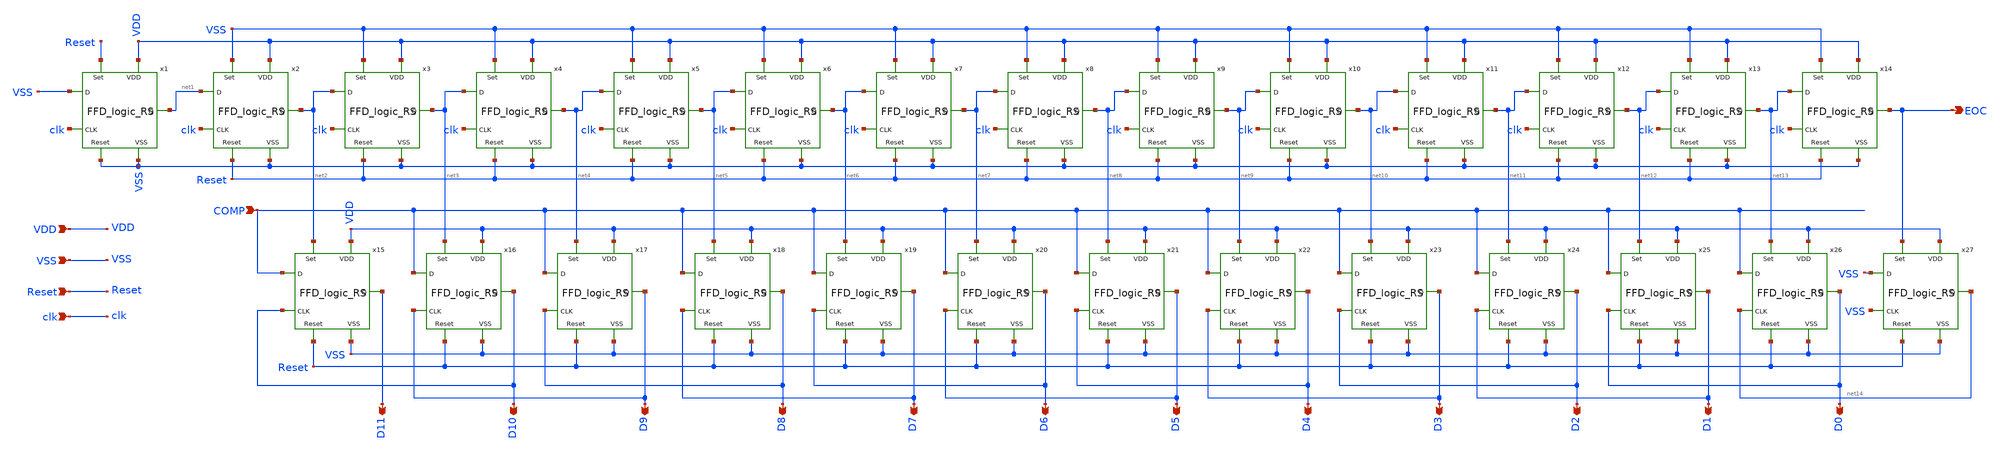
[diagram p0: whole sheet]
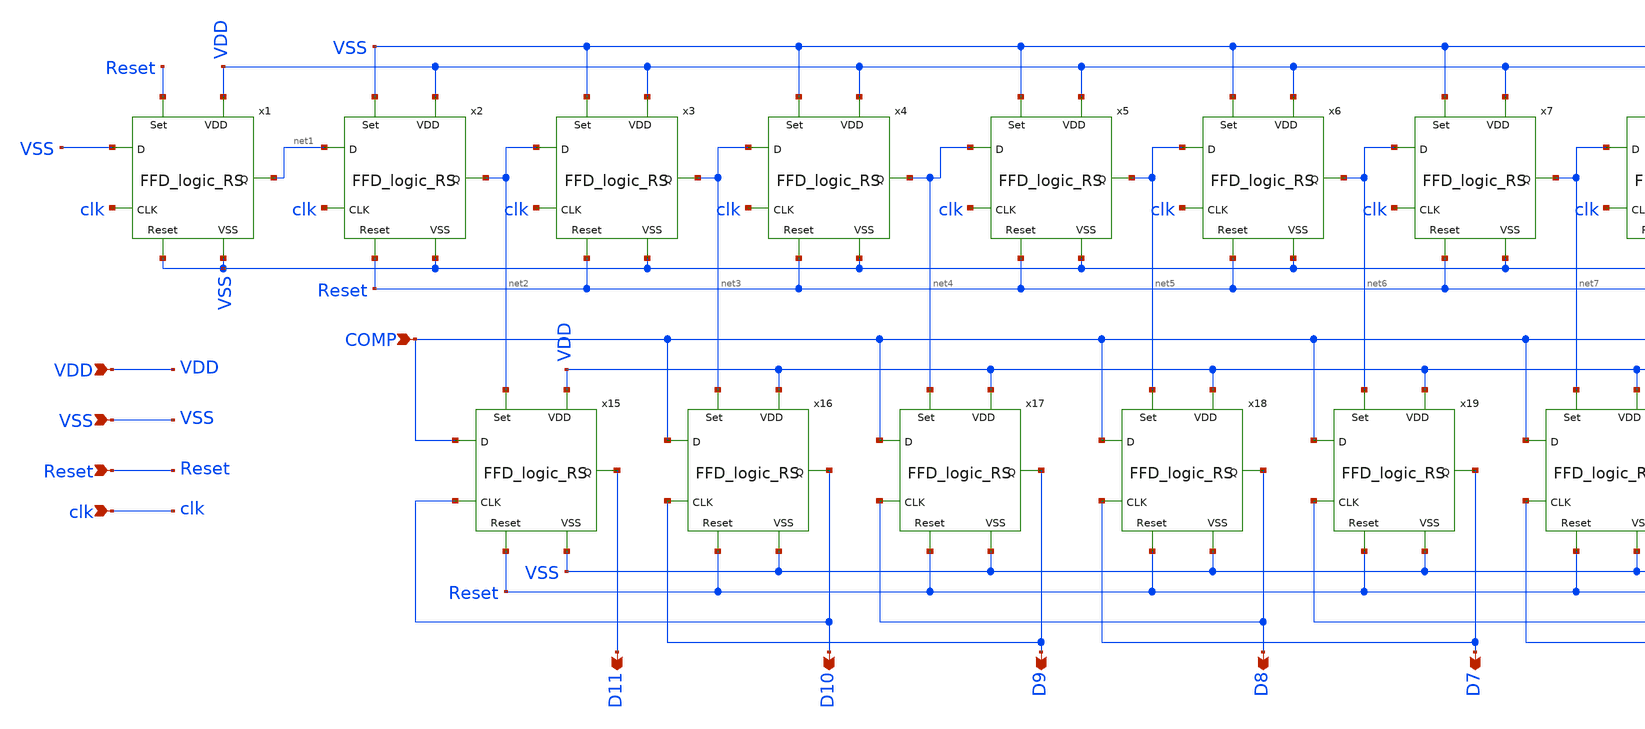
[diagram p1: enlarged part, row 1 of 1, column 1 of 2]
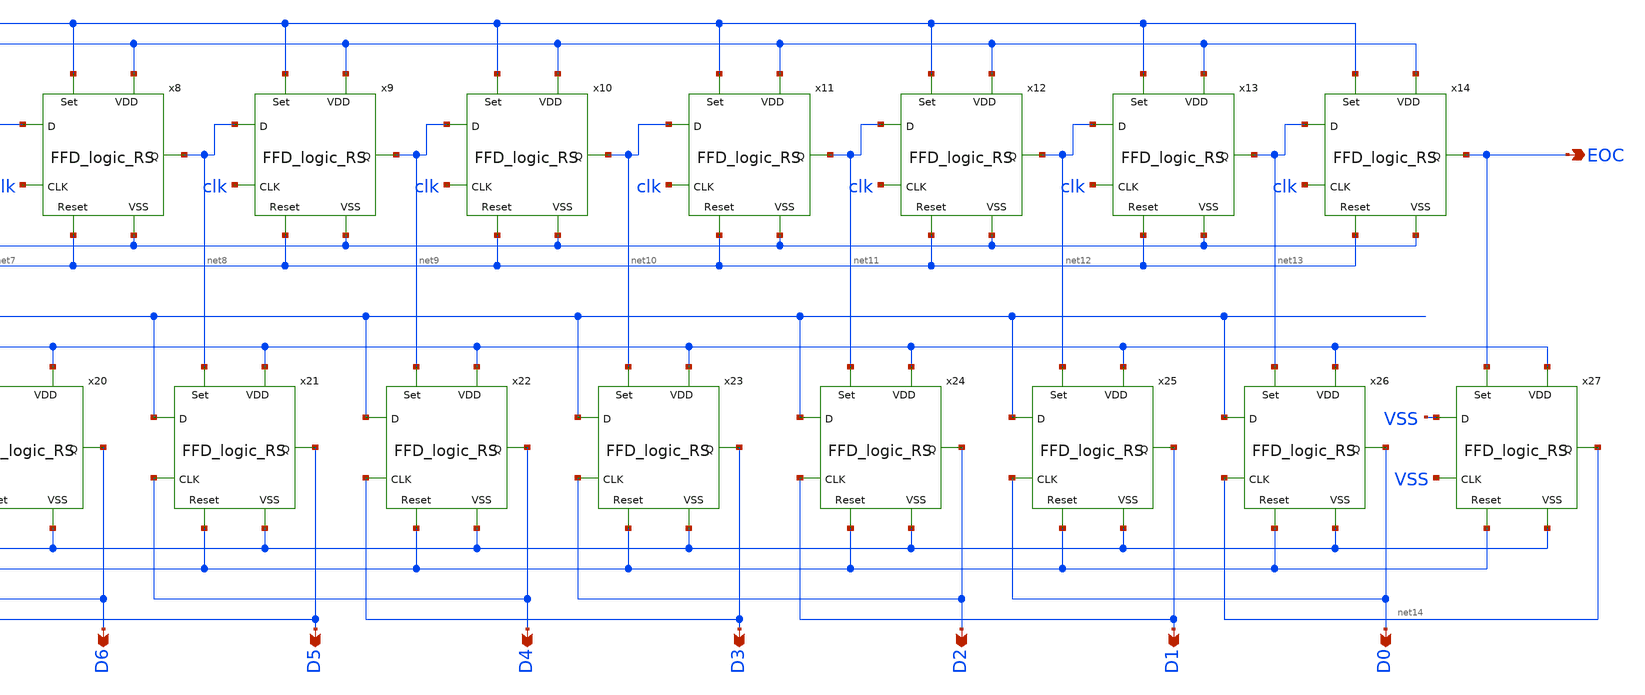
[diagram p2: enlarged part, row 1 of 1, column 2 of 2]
** sch_path: SAR_Logic_new.sch
**.subckt SAR_Logic_new VDD VSS COMP Reset clk D11 D10 D9 D8 D7 D6 D5 D4 D3 D2 D1 D0 EOC
*.ipin VDD
*.ipin VSS
*.ipin COMP
*.ipin Reset
*.ipin clk
*.opin D11
*.opin D10
*.opin D9
*.opin D8
*.opin D7
*.opin D6
*.opin D5
*.opin D4
*.opin D3
*.opin D2
*.opin D1
*.opin D0
*.opin EOC
x1 Reset VDD net1 clk VSS VSS VSS FFD_logic_RS
x2 VSS VDD net2 clk net1 VSS Reset FFD_logic_RS
x3 VSS VDD net3 clk net2 VSS Reset FFD_logic_RS
x4 VSS VDD net4 clk net3 VSS Reset FFD_logic_RS
x5 VSS VDD net5 clk net4 VSS Reset FFD_logic_RS
x6 VSS VDD net6 clk net5 VSS Reset FFD_logic_RS
x7 VSS VDD net7 clk net6 VSS Reset FFD_logic_RS
x8 VSS VDD net8 clk net7 VSS Reset FFD_logic_RS
x9 VSS VDD net9 clk net8 VSS Reset FFD_logic_RS
x10 VSS VDD net10 clk net9 VSS Reset FFD_logic_RS
x11 VSS VDD net11 clk net10 VSS Reset FFD_logic_RS
x12 VSS VDD net12 clk net11 VSS Reset FFD_logic_RS
x13 VSS VDD net13 clk net12 VSS Reset FFD_logic_RS
x14 VSS VDD EOC clk net13 VSS Reset FFD_logic_RS
x15 net2 VDD D11 D10 COMP VSS Reset FFD_logic_RS
x16 net3 VDD D10 D9 COMP VSS Reset FFD_logic_RS
x17 net4 VDD D9 D8 COMP VSS Reset FFD_logic_RS
x18 net5 VDD D8 D7 COMP VSS Reset FFD_logic_RS
x19 net6 VDD D7 D6 COMP VSS Reset FFD_logic_RS
x20 net7 VDD D6 D5 COMP VSS Reset FFD_logic_RS
x21 net8 VDD D5 D4 COMP VSS Reset FFD_logic_RS
x22 net9 VDD D4 D3 COMP VSS Reset FFD_logic_RS
x23 net10 VDD D3 D2 COMP VSS Reset FFD_logic_RS
x24 net11 VDD D2 D1 COMP VSS Reset FFD_logic_RS
x25 net12 VDD D1 D0 COMP VSS Reset FFD_logic_RS
x26 net13 VDD D0 net14 COMP VSS Reset FFD_logic_RS
x27 EOC VDD net14 VSS VSS VSS Reset FFD_logic_RS
**.ends

* expanding   symbol:  Thesis/FFD_logic_RS.sym # of pins=7
** sym_path: FFD_logic_RS.sym
** sch_path: FFD_logic_RS.sch
.subckt FFD_logic_RS Set VDD Q CLK D VSS Reset
*.ipin D
*.ipin CLK
*.ipin VDD
*.ipin VSS
*.opin Q
*.ipin Set
*.ipin Reset
x1 VDD net3 D net2 VSS nand_FFD
x2 VDD net4 net2 net1 VSS nand_FFD
x5 VDD net8 net5 CLK VSS nand_FFD
x6 VDD net7 CLK net6 VSS nand_FFD
x9 VDD D net1 VSS Inverter
x10 VDD CLK net2 VSS Inverter
x3 net6 VDD net5 net10 net3 VSS nand_FFD_3pin
x4 net11 VDD net6 net5 net4 VSS nand_FFD_3pin
x7 net9 VDD Q net10 net8 VSS nand_FFD_3pin
x8 net11 VDD net9 Q net7 VSS nand_FFD_3pin
x11 VDD Set net10 VSS Inverter
x12 VDD Reset net11 VSS Inverter
.ends


* expanding   symbol:  nand_FFD.sym # of pins=5
** sym_path: nand_FFD.sym
** sch_path: nand_FFD.sch
.subckt nand_FFD VDD Y A B VSS
*.ipin VDD
*.ipin A
*.ipin B
*.ipin VSS
*.opin Y
XM1 Y A net1 VSS sky130_fd_pr__nfet_01v8 L=0.15 W=1 nf=1 ad='int((nf+1)/2) * W/nf * 0.29' as='int((nf+2)/2) * W/nf * 0.29'
+ pd='2*int((nf+1)/2) * (W/nf + 0.29)' ps='2*int((nf+2)/2) * (W/nf + 0.29)' nrd='0.29 / W' nrs='0.29 / W'
+ sa=0 sb=0 sd=0 mult=1 m=1
XM2 net1 B VSS VSS sky130_fd_pr__nfet_01v8 L=0.15 W=1 nf=1 ad='int((nf+1)/2) * W/nf * 0.29' as='int((nf+2)/2) * W/nf * 0.29'
+ pd='2*int((nf+1)/2) * (W/nf + 0.29)' ps='2*int((nf+2)/2) * (W/nf + 0.29)' nrd='0.29 / W' nrs='0.29 / W'
+ sa=0 sb=0 sd=0 mult=1 m=1
XM3 Y A VDD VDD sky130_fd_pr__pfet_01v8 L=0.15 W=2 nf=1 ad='int((nf+1)/2) * W/nf * 0.29' as='int((nf+2)/2) * W/nf * 0.29'
+ pd='2*int((nf+1)/2) * (W/nf + 0.29)' ps='2*int((nf+2)/2) * (W/nf + 0.29)' nrd='0.29 / W' nrs='0.29 / W'
+ sa=0 sb=0 sd=0 mult=1 m=1
XM4 Y B VDD VDD sky130_fd_pr__pfet_01v8 L=0.15 W=2 nf=1 ad='int((nf+1)/2) * W/nf * 0.29' as='int((nf+2)/2) * W/nf * 0.29'
+ pd='2*int((nf+1)/2) * (W/nf + 0.29)' ps='2*int((nf+2)/2) * (W/nf + 0.29)' nrd='0.29 / W' nrs='0.29 / W'
+ sa=0 sb=0 sd=0 mult=1 m=1
.ends


* expanding   symbol:  Inverter.sym # of pins=4
** sym_path: Inverter.sym
** sch_path: Inverter.sch
.subckt Inverter VDD IN OUT VSS
*.ipin IN
*.ipin VSS
*.ipin VDD
*.opin OUT
XM1 OUT IN VSS VSS sky130_fd_pr__nfet_01v8 L=0.3 W=1 nf=1 ad='int((nf+1)/2) * W/nf * 0.29' as='int((nf+2)/2) * W/nf * 0.29'
+ pd='2*int((nf+1)/2) * (W/nf + 0.29)' ps='2*int((nf+2)/2) * (W/nf + 0.29)' nrd='0.29 / W' nrs='0.29 / W'
+ sa=0 sb=0 sd=0 mult=1 m=1
XM2 OUT IN VDD VDD sky130_fd_pr__pfet_01v8 L=0.3 W=2 nf=1 ad='int((nf+1)/2) * W/nf * 0.29' as='int((nf+2)/2) * W/nf * 0.29'
+ pd='2*int((nf+1)/2) * (W/nf + 0.29)' ps='2*int((nf+2)/2) * (W/nf + 0.29)' nrd='0.29 / W' nrs='0.29 / W'
+ sa=0 sb=0 sd=0 mult=1 m=1
.ends


* expanding   symbol:  Thesis/nand_FFD_3pin.sym # of pins=6
** sym_path: nand_FFD_3pin.sym
** sch_path: nand_FFD_3pin.sch
.subckt nand_FFD_3pin C VDD Y A B VSS
*.ipin VDD
*.ipin A
*.ipin B
*.ipin VSS
*.opin Y
*.ipin C
XM1 Y A net1 VSS sky130_fd_pr__nfet_01v8 L=0.15 W=1 nf=1 ad='int((nf+1)/2) * W/nf * 0.29' as='int((nf+2)/2) * W/nf * 0.29'
+ pd='2*int((nf+1)/2) * (W/nf + 0.29)' ps='2*int((nf+2)/2) * (W/nf + 0.29)' nrd='0.29 / W' nrs='0.29 / W'
+ sa=0 sb=0 sd=0 mult=1 m=1
XM2 net1 B net2 VSS sky130_fd_pr__nfet_01v8 L=0.15 W=1 nf=1 ad='int((nf+1)/2) * W/nf * 0.29' as='int((nf+2)/2) * W/nf * 0.29'
+ pd='2*int((nf+1)/2) * (W/nf + 0.29)' ps='2*int((nf+2)/2) * (W/nf + 0.29)' nrd='0.29 / W' nrs='0.29 / W'
+ sa=0 sb=0 sd=0 mult=1 m=1
XM3 Y A VDD VDD sky130_fd_pr__pfet_01v8 L=0.15 W=2 nf=1 ad='int((nf+1)/2) * W/nf * 0.29' as='int((nf+2)/2) * W/nf * 0.29'
+ pd='2*int((nf+1)/2) * (W/nf + 0.29)' ps='2*int((nf+2)/2) * (W/nf + 0.29)' nrd='0.29 / W' nrs='0.29 / W'
+ sa=0 sb=0 sd=0 mult=1 m=1
XM4 Y B VDD VDD sky130_fd_pr__pfet_01v8 L=0.15 W=2 nf=1 ad='int((nf+1)/2) * W/nf * 0.29' as='int((nf+2)/2) * W/nf * 0.29'
+ pd='2*int((nf+1)/2) * (W/nf + 0.29)' ps='2*int((nf+2)/2) * (W/nf + 0.29)' nrd='0.29 / W' nrs='0.29 / W'
+ sa=0 sb=0 sd=0 mult=1 m=1
XM5 Y C VDD VDD sky130_fd_pr__pfet_01v8 L=0.15 W=2 nf=1 ad='int((nf+1)/2) * W/nf * 0.29' as='int((nf+2)/2) * W/nf * 0.29'
+ pd='2*int((nf+1)/2) * (W/nf + 0.29)' ps='2*int((nf+2)/2) * (W/nf + 0.29)' nrd='0.29 / W' nrs='0.29 / W'
+ sa=0 sb=0 sd=0 mult=1 m=1
XM6 net2 C VSS VSS sky130_fd_pr__nfet_01v8 L=0.15 W=1 nf=1 ad='int((nf+1)/2) * W/nf * 0.29' as='int((nf+2)/2) * W/nf * 0.29'
+ pd='2*int((nf+1)/2) * (W/nf + 0.29)' ps='2*int((nf+2)/2) * (W/nf + 0.29)' nrd='0.29 / W' nrs='0.29 / W'
+ sa=0 sb=0 sd=0 mult=1 m=1
.ends

.end
